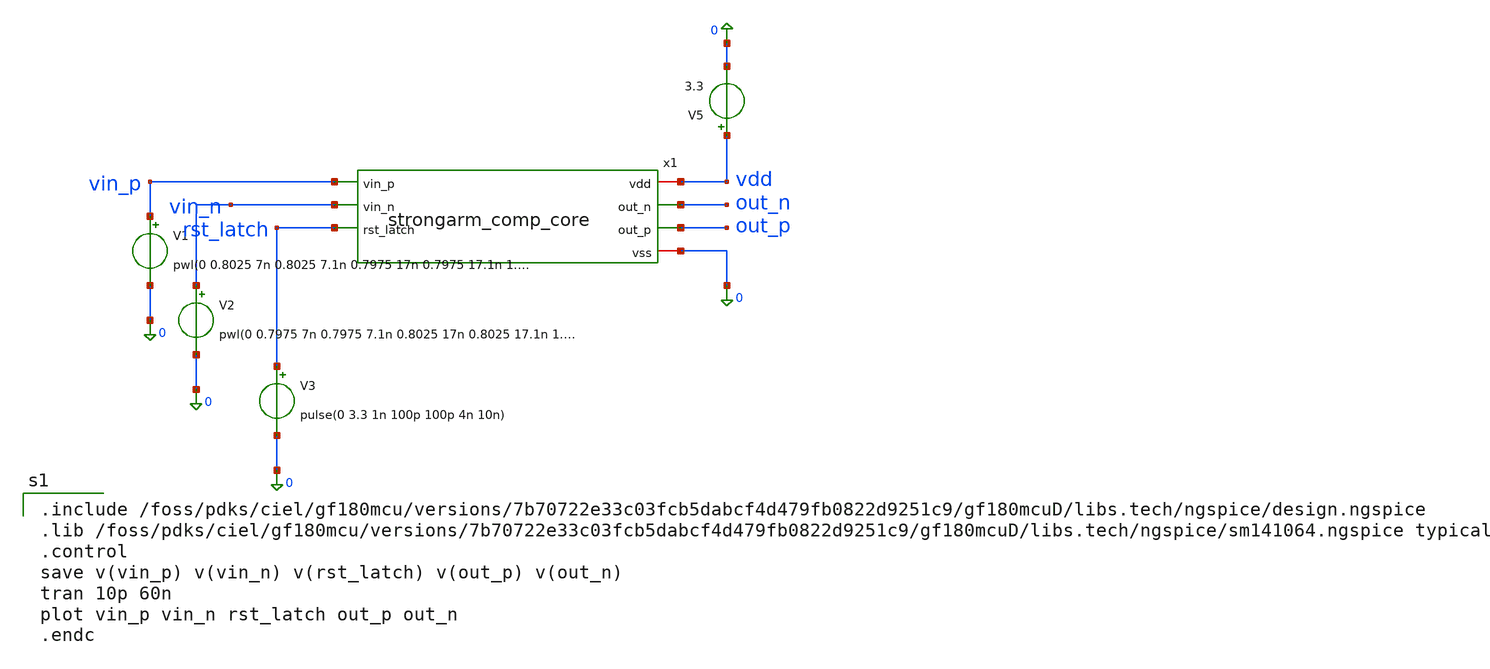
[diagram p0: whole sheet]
** sch_path: xschem/sar_adc/blocks/comparator/testbench/tb_strongarm_comp_core.sch
**.subckt tb_strongarm_comp_core
x1 vdd out_n out_p vin_p vin_n rst_latch 0 strongarm_comp_core
V1 vin_p 0 pwl(0 0.8025 7n 0.8025 7.1n 0.7975 17n 0.7975 17.1n 1.6525 27n 1.6525 27.1n 1.6475 37n
+ 1.6475 37.1n 2.5025 40n 2.5025)
V2 vin_n 0 pwl(0 0.7975 7n 0.7975 7.1n 0.8025 17n 0.8025 17.1n 1.6475 27n 1.6475 27.1n 1.6525 37n
+ 1.6525 37.1n 2.4975 40n 2.4975)
V3 rst_latch 0 pulse(0 3.3 1n 100p 100p 4n 10n)
V5 vdd 0 3.3
**** begin user architecture code

.include /foss/pdks/ciel/gf180mcu/versions/7b70722e33c03fcb5dabcf4d479fb0822d9251c9/gf180mcuD/libs.tech/ngspice/design.ngspice
.lib /foss/pdks/ciel/gf180mcu/versions/7b70722e33c03fcb5dabcf4d479fb0822d9251c9/gf180mcuD/libs.tech/ngspice/sm141064.ngspice typical
.control
save v(vin_p) v(vin_n) v(rst_latch) v(out_p) v(out_n)
tran 10p 60n
plot vin_p vin_n rst_latch out_p out_n
.endc

**** end user architecture code
**.ends

* expanding   symbol:  sar_adc/blocks/comparator/strongarm_comp_core.sym # of pins=7
** sym_path: xschem/sar_adc/blocks/comparator/strongarm_comp_core.sym
** sch_path: xschem/sar_adc/blocks/comparator/strongarm_comp_core.sch
.subckt strongarm_comp_core vdd out_n out_p vin_p vin_n rst_latch vss
*.ipin vin_p
*.ipin vin_n
*.ipin rst_latch
*.iopin vdd
*.iopin vss
*.opin out_p
*.opin out_n
XMtail net1 rst_latch vss vss nfet_03v3 L=0.28u W=0.50u nf=1 ad='int((nf+1)/2) * W/nf * 0.18u' as='int((nf+2)/2) * W/nf * 0.18u'
+ pd='2*int((nf+1)/2) * (W/nf + 0.18u)' ps='2*int((nf+2)/2) * (W/nf + 0.18u)' nrd='0.18u / W' nrs='0.18u / W'
+ sa=0 sb=0 sd=0 m=1
XM1 net2 vin_p net1 vss nfet_03v3 L=0.28u W=0.42u nf=1 ad='int((nf+1)/2) * W/nf * 0.18u' as='int((nf+2)/2) * W/nf * 0.18u'
+ pd='2*int((nf+1)/2) * (W/nf + 0.18u)' ps='2*int((nf+2)/2) * (W/nf + 0.18u)' nrd='0.18u / W' nrs='0.18u / W'
+ sa=0 sb=0 sd=0 m=1
XM2 net3 vin_n net1 vss nfet_03v3 L=0.28u W=0.42u nf=1 ad='int((nf+1)/2) * W/nf * 0.18u' as='int((nf+2)/2) * W/nf * 0.18u'
+ pd='2*int((nf+1)/2) * (W/nf + 0.18u)' ps='2*int((nf+2)/2) * (W/nf + 0.18u)' nrd='0.18u / W' nrs='0.18u / W'
+ sa=0 sb=0 sd=0 m=1
XM3 out_p out_n net2 vss nfet_03v3 L=0.28u W=0.42u nf=1 ad='int((nf+1)/2) * W/nf * 0.18u' as='int((nf+2)/2) * W/nf * 0.18u'
+ pd='2*int((nf+1)/2) * (W/nf + 0.18u)' ps='2*int((nf+2)/2) * (W/nf + 0.18u)' nrd='0.18u / W' nrs='0.18u / W'
+ sa=0 sb=0 sd=0 m=1
XM4 out_n out_p net3 vss nfet_03v3 L=0.28u W=0.42u nf=1 ad='int((nf+1)/2) * W/nf * 0.18u' as='int((nf+2)/2) * W/nf * 0.18u'
+ pd='2*int((nf+1)/2) * (W/nf + 0.18u)' ps='2*int((nf+2)/2) * (W/nf + 0.18u)' nrd='0.18u / W' nrs='0.18u / W'
+ sa=0 sb=0 sd=0 m=1
XM5 out_p out_n vdd vdd pfet_03v3 L=0.28u W=0.42u nf=1 ad='int((nf+1)/2) * W/nf * 0.18u' as='int((nf+2)/2) * W/nf * 0.18u'
+ pd='2*int((nf+1)/2) * (W/nf + 0.18u)' ps='2*int((nf+2)/2) * (W/nf + 0.18u)' nrd='0.18u / W' nrs='0.18u / W'
+ sa=0 sb=0 sd=0 m=1
XM6 out_n out_p vdd vdd pfet_03v3 L=0.28u W=0.42u nf=1 ad='int((nf+1)/2) * W/nf * 0.18u' as='int((nf+2)/2) * W/nf * 0.18u'
+ pd='2*int((nf+1)/2) * (W/nf + 0.18u)' ps='2*int((nf+2)/2) * (W/nf + 0.18u)' nrd='0.18u / W' nrs='0.18u / W'
+ sa=0 sb=0 sd=0 m=1
XM7 out_p rst_latch vdd vdd pfet_03v3 L=0.28u W=0.42u nf=1 ad='int((nf+1)/2) * W/nf * 0.18u' as='int((nf+2)/2) * W/nf * 0.18u'
+ pd='2*int((nf+1)/2) * (W/nf + 0.18u)' ps='2*int((nf+2)/2) * (W/nf + 0.18u)' nrd='0.18u / W' nrs='0.18u / W'
+ sa=0 sb=0 sd=0 m=1
XM8 out_n rst_latch vdd vdd pfet_03v3 L=0.28u W=0.42u nf=1 ad='int((nf+1)/2) * W/nf * 0.18u' as='int((nf+2)/2) * W/nf * 0.18u'
+ pd='2*int((nf+1)/2) * (W/nf + 0.18u)' ps='2*int((nf+2)/2) * (W/nf + 0.18u)' nrd='0.18u / W' nrs='0.18u / W'
+ sa=0 sb=0 sd=0 m=1
XM9 net2 rst_latch vdd vdd pfet_03v3 L=0.28u W=0.42u nf=1 ad='int((nf+1)/2) * W/nf * 0.18u' as='int((nf+2)/2) * W/nf * 0.18u'
+ pd='2*int((nf+1)/2) * (W/nf + 0.18u)' ps='2*int((nf+2)/2) * (W/nf + 0.18u)' nrd='0.18u / W' nrs='0.18u / W'
+ sa=0 sb=0 sd=0 m=1
XM10 net3 rst_latch vdd vdd pfet_03v3 L=0.28u W=0.42u nf=1 ad='int((nf+1)/2) * W/nf * 0.18u' as='int((nf+2)/2) * W/nf * 0.18u'
+ pd='2*int((nf+1)/2) * (W/nf + 0.18u)' ps='2*int((nf+2)/2) * (W/nf + 0.18u)' nrd='0.18u / W' nrs='0.18u / W'
+ sa=0 sb=0 sd=0 m=1
.ends

.end
